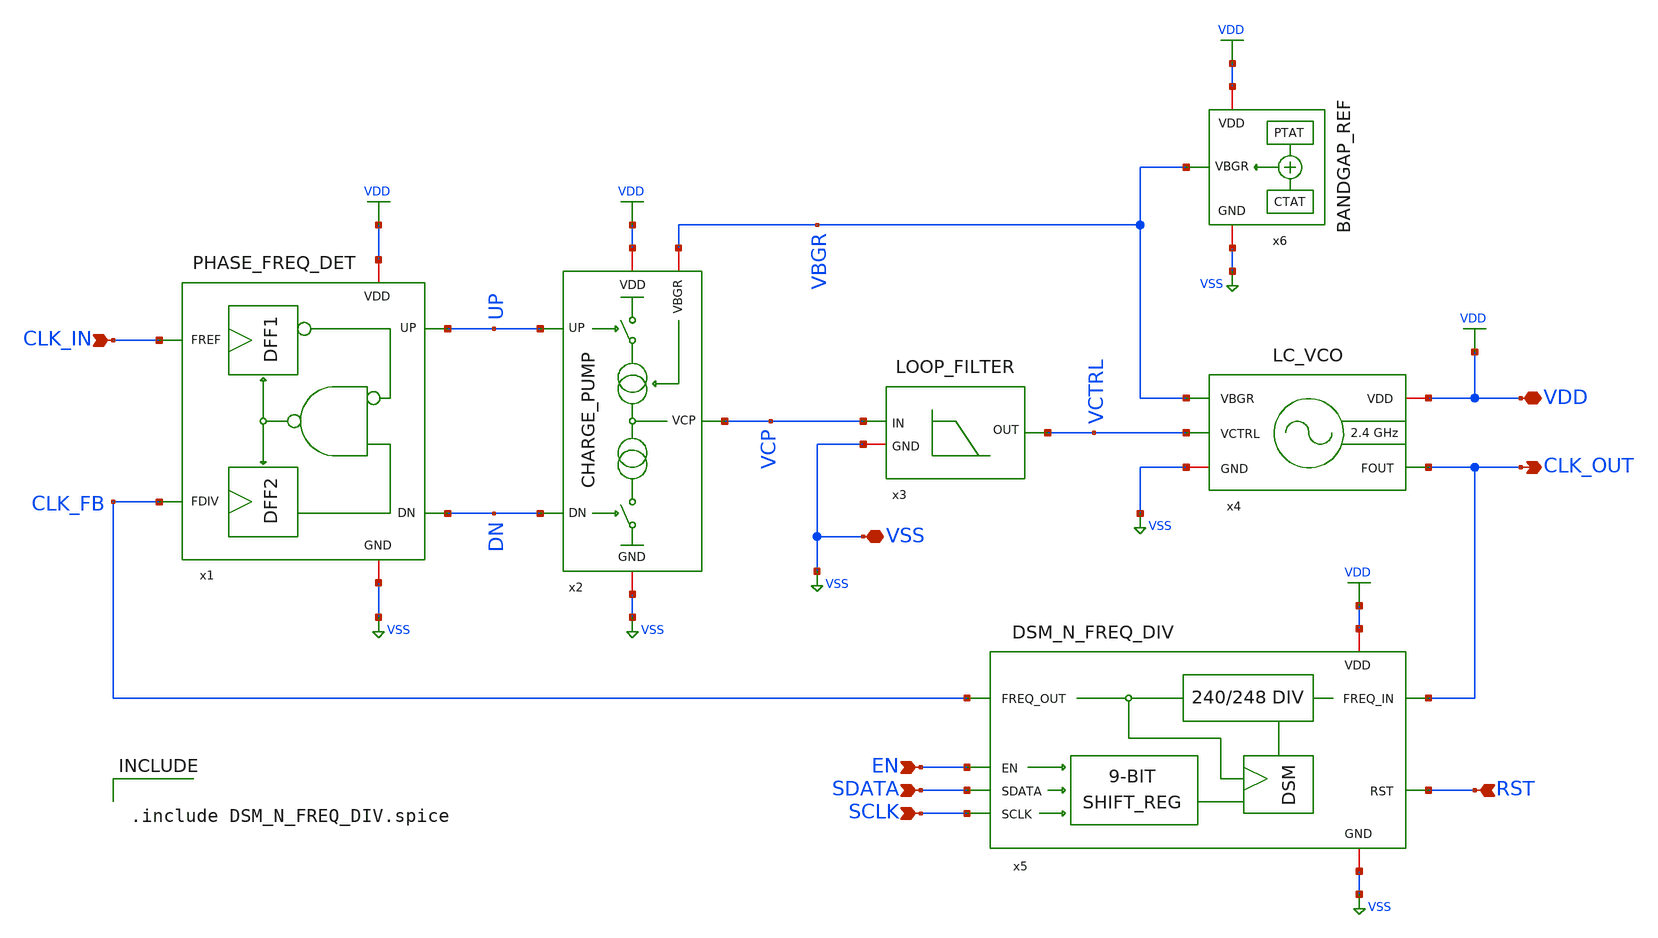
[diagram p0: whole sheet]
** sch_path: xschem/LC_VCO_FPLL.sch
**.subckt LC_VCO_FPLL CLK_IN CLK_OUT EN SDATA SCLK RST VDD VSS
*.ipin CLK_IN
*.opin CLK_OUT
*.ipin EN
*.ipin SDATA
*.ipin SCLK
*.ipin RST
*.iopin VDD
*.iopin VSS
x1 CLK_IN UP VDD VSS CLK_FB DN PHASE_FREQ_DET
x2 UP VDD VCP VBGR VSS DN CHARGE_PUMP
x3 VCTRL VCP VSS LOOP_FILTER
x4 VDD VCTRL VSS CLK_OUT VBGR LC_VCO
x5 [ CLK_OUT RST SCLK SDATA EN ] [ CLK_FB ] null dut
.model dut d_cosim simulation=../simulations/dsm_and_freq_divider.so
x6 VDD VSS VBGR BANDGAP_REF
**** begin user architecture code


.include DSM_N_FREQ_DIV.spice


**** end user architecture code
**.ends
.GLOBAL VSS
.GLOBAL VDD
.end
